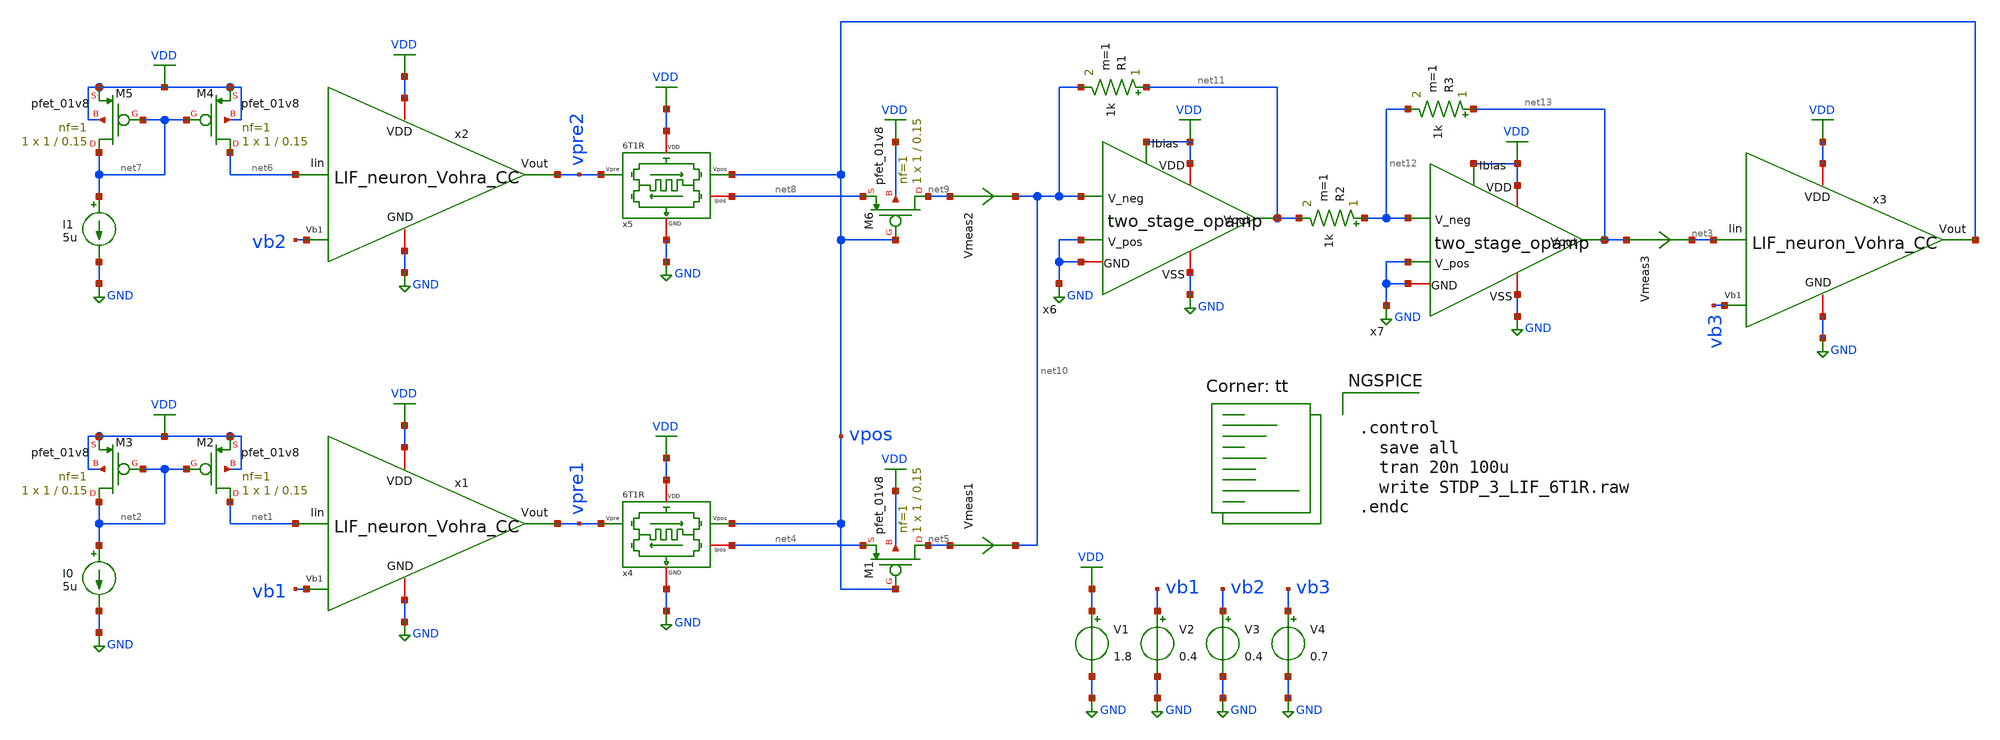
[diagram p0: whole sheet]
** sch_path: STDP/STDP_3_LIF_6T1R_opamps.sch
**.subckt STDP_3_LIF_6T1R_opamps
V1 VDD GND 1.8
V2 vb1 GND 0.4
x4 VDD net4 vpre1 vpos GND 6T1R
x1 VDD vpre1 vb1 GND net1 LIF_neuron_Vohra_CC
I0 net2 GND 5u
XM2 net1 net2 VDD VDD sky130_fd_pr__pfet_01v8 L=0.15 W=1 nf=1 ad='int((nf+1)/2) * W/nf * 0.29' as='int((nf+2)/2) * W/nf * 0.29'
+ pd='2*int((nf+1)/2) * (W/nf + 0.29)' ps='2*int((nf+2)/2) * (W/nf + 0.29)' nrd='0.29 / W' nrs='0.29 / W'
+ sa=0 sb=0 sd=0 mult=1 m=1
XM3 net2 net2 VDD VDD sky130_fd_pr__pfet_01v8 L=0.15 W=1 nf=1 ad='int((nf+1)/2) * W/nf * 0.29' as='int((nf+2)/2) * W/nf * 0.29'
+ pd='2*int((nf+1)/2) * (W/nf + 0.29)' ps='2*int((nf+2)/2) * (W/nf + 0.29)' nrd='0.29 / W' nrs='0.29 / W'
+ sa=0 sb=0 sd=0 mult=1 m=1
x3 VDD vpos vb3 GND net3 LIF_neuron_Vohra_CC
XM1 net5 vpos net4 VDD sky130_fd_pr__pfet_01v8 L=0.15 W=1 nf=1 ad='int((nf+1)/2) * W/nf * 0.29' as='int((nf+2)/2) * W/nf * 0.29'
+ pd='2*int((nf+1)/2) * (W/nf + 0.29)' ps='2*int((nf+2)/2) * (W/nf + 0.29)' nrd='0.29 / W' nrs='0.29 / W'
+ sa=0 sb=0 sd=0 mult=1 m=1
Vmeas1 net5 net10 0
.save i(vmeas1)
V3 vb2 GND 0.4
x5 VDD net8 vpre2 vpos GND 6T1R
x2 VDD vpre2 vb2 GND net6 LIF_neuron_Vohra_CC
I1 net7 GND 5u
XM4 net6 net7 VDD VDD sky130_fd_pr__pfet_01v8 L=0.15 W=1 nf=1 ad='int((nf+1)/2) * W/nf * 0.29' as='int((nf+2)/2) * W/nf * 0.29'
+ pd='2*int((nf+1)/2) * (W/nf + 0.29)' ps='2*int((nf+2)/2) * (W/nf + 0.29)' nrd='0.29 / W' nrs='0.29 / W'
+ sa=0 sb=0 sd=0 mult=1 m=1
XM5 net7 net7 VDD VDD sky130_fd_pr__pfet_01v8 L=0.15 W=1 nf=1 ad='int((nf+1)/2) * W/nf * 0.29' as='int((nf+2)/2) * W/nf * 0.29'
+ pd='2*int((nf+1)/2) * (W/nf + 0.29)' ps='2*int((nf+2)/2) * (W/nf + 0.29)' nrd='0.29 / W' nrs='0.29 / W'
+ sa=0 sb=0 sd=0 mult=1 m=1
XM6 net9 vpos net8 VDD sky130_fd_pr__pfet_01v8 L=0.15 W=1 nf=1 ad='int((nf+1)/2) * W/nf * 0.29' as='int((nf+2)/2) * W/nf * 0.29'
+ pd='2*int((nf+1)/2) * (W/nf + 0.29)' ps='2*int((nf+2)/2) * (W/nf + 0.29)' nrd='0.29 / W' nrs='0.29 / W'
+ sa=0 sb=0 sd=0 mult=1 m=1
Vmeas2 net9 net10 0
.save i(vmeas2)
V4 vb3 GND 0.7
x6 VDD net11 VDD net10 GND GND GND two_stage_opamp W1=15 W2=94 W3=3 W4=4.5 W5=14 W6=10 L1=0.15
+ L2=0.15 L3=0.15 L4=0.15 L5=0.15 L6=0.15
R1 net11 net10 1k m=1
R2 net12 net11 1k m=1
x7 VDD net13 VDD net12 GND GND GND two_stage_opamp W1=15 W2=94 W3=3 W4=4.5 W5=14 W6=10 L1=0.15
+ L2=0.15 L3=0.15 L4=0.15 L5=0.15 L6=0.15
R3 net13 net12 1k m=1
Vmeas3 net13 net3 0
.save i(vmeas3)
**** begin user architecture code
.lib $::SKYWATER_MODELS/sky130.lib.spice tt

** opencircuitdesign pdks install
.inc $::SKYWATER_MODELS/rram_v0.spice



.control
  save all
  tran 20n 100u
  write STDP_3_LIF_6T1R.raw
.endc


**** end user architecture code
**.ends

* expanding   symbol:  /home/ricardoatt/RATT_repos/Proyectos_xschem/synapse/6T1R.sym # of pins=5
** sym_path: synapse/6T1R.sym
** sch_path: synapse/6T1R.sch
.subckt 6T1R VDD Ipos Vpre Vpos GND
*.ipin Vpre
*.ipin Vpos
*.iopin GND
*.iopin Ipos
*.iopin VDD
XM1 vipre Vpre net1 GND sky130_fd_pr__nfet_01v8 L=0.15 W=10 nf=1 ad='int((nf+1)/2) * W/nf * 0.29' as='int((nf+2)/2) * W/nf * 0.29'
+ pd='2*int((nf+1)/2) * (W/nf + 0.29)' ps='2*int((nf+2)/2) * (W/nf + 0.29)' nrd='0.29 / W' nrs='0.29 / W'
+ sa=0 sb=0 sd=0 mult=1 m=1
XR1 net2 net1 rram_v0
XM3 vipre Vpos net2 GND sky130_fd_pr__nfet_01v8 L=0.15 W=1 nf=1 ad='int((nf+1)/2) * W/nf * 0.29' as='int((nf+2)/2) * W/nf * 0.29'
+ pd='2*int((nf+1)/2) * (W/nf + 0.29)' ps='2*int((nf+2)/2) * (W/nf + 0.29)' nrd='0.29 / W' nrs='0.29 / W'
+ sa=0 sb=0 sd=0 mult=1 m=1
XM6 Ipos vipre VDD VDD sky130_fd_pr__pfet_01v8 L=0.15 W=1 nf=1 ad='int((nf+1)/2) * W/nf * 0.29' as='int((nf+2)/2) * W/nf * 0.29'
+ pd='2*int((nf+1)/2) * (W/nf + 0.29)' ps='2*int((nf+2)/2) * (W/nf + 0.29)' nrd='0.29 / W' nrs='0.29 / W'
+ sa=0 sb=0 sd=0 mult=1 m=1
XM5 vipre vipre VDD VDD sky130_fd_pr__pfet_01v8 L=0.15 W=20 nf=1 ad='int((nf+1)/2) * W/nf * 0.29' as='int((nf+2)/2) * W/nf * 0.29'
+ pd='2*int((nf+1)/2) * (W/nf + 0.29)' ps='2*int((nf+2)/2) * (W/nf + 0.29)' nrd='0.29 / W' nrs='0.29 / W'
+ sa=0 sb=0 sd=0 mult=1 m=1
XM2 net1 Vpos GND GND sky130_fd_pr__nfet_01v8 L=0.15 W=1 nf=1 ad='int((nf+1)/2) * W/nf * 0.29' as='int((nf+2)/2) * W/nf * 0.29'
+ pd='2*int((nf+1)/2) * (W/nf + 0.29)' ps='2*int((nf+2)/2) * (W/nf + 0.29)' nrd='0.29 / W' nrs='0.29 / W'
+ sa=0 sb=0 sd=0 mult=1 m=1
XM4 net2 Vpre GND GND sky130_fd_pr__nfet_01v8 L=0.15 W=10 nf=1 ad='int((nf+1)/2) * W/nf * 0.29' as='int((nf+2)/2) * W/nf * 0.29'
+ pd='2*int((nf+1)/2) * (W/nf + 0.29)' ps='2*int((nf+2)/2) * (W/nf + 0.29)' nrd='0.29 / W' nrs='0.29 / W'
+ sa=0 sb=0 sd=0 mult=1 m=1
.ends


* expanding   symbol:
*+  /home/ricardoatt/RATT_repos/Proyectos_xschem/LIF_neuron/LIF_neuron_Vohra_CC.sym # of pins=5
** sym_path: LIF_neuron/LIF_neuron_Vohra_CC.sym
** sch_path: LIF_neuron/LIF_neuron_Vohra_CC.sch
.subckt LIF_neuron_Vohra_CC VDD Vout Vb1 GND Iin
*.iopin GND
*.ipin Vb1
*.iopin VDD
*.opin Vout
*.ipin Iin
XM13 net2 Vb1 GND GND sky130_fd_pr__nfet_01v8 L=0.5 W=5 nf=1 ad='int((nf+1)/2) * W/nf * 0.29' as='int((nf+2)/2) * W/nf * 0.29'
+ pd='2*int((nf+1)/2) * (W/nf + 0.29)' ps='2*int((nf+2)/2) * (W/nf + 0.29)' nrd='0.29 / W' nrs='0.29 / W'
+ sa=0 sb=0 sd=0 mult=1 m=1
XM12 rc net1 net2 GND sky130_fd_pr__nfet_01v8 L=1 W=1 nf=1 ad='int((nf+1)/2) * W/nf * 0.29' as='int((nf+2)/2) * W/nf * 0.29'
+ pd='2*int((nf+1)/2) * (W/nf + 0.29)' ps='2*int((nf+2)/2) * (W/nf + 0.29)' nrd='0.29 / W' nrs='0.29 / W'
+ sa=0 sb=0 sd=0 mult=1 m=1
XM11 rc net1 VDD VDD sky130_fd_pr__pfet_01v8 L=1 W=1 nf=1 ad='int((nf+1)/2) * W/nf * 0.29' as='int((nf+2)/2) * W/nf * 0.29'
+ pd='2*int((nf+1)/2) * (W/nf + 0.29)' ps='2*int((nf+2)/2) * (W/nf + 0.29)' nrd='0.29 / W' nrs='0.29 / W'
+ sa=0 sb=0 sd=0 mult=1 m=1
XC1 rc GND sky130_fd_pr__cap_mim_m3_1 W=21 L=1 MF=1 m=1
XM14 Iin rc GND GND sky130_fd_pr__nfet_01v8 L=10 W=1 nf=1 ad='int((nf+1)/2) * W/nf * 0.29' as='int((nf+2)/2) * W/nf * 0.29'
+ pd='2*int((nf+1)/2) * (W/nf + 0.29)' ps='2*int((nf+2)/2) * (W/nf + 0.29)' nrd='0.29 / W' nrs='0.29 / W'
+ sa=0 sb=0 sd=0 mult=1 m=1
XC2 Iin GND sky130_fd_pr__cap_mim_m3_1 W=10 L=1 MF=50 m=50
XM6 net3 Vout GND GND sky130_fd_pr__nfet_01v8 L=0.5 W=1 nf=1 ad='int((nf+1)/2) * W/nf * 0.29' as='int((nf+2)/2) * W/nf * 0.29'
+ pd='2*int((nf+1)/2) * (W/nf + 0.29)' ps='2*int((nf+2)/2) * (W/nf + 0.29)' nrd='0.29 / W' nrs='0.29 / W'
+ sa=0 sb=0 sd=0 mult=1 m=1
XM7 net1 Iin net3 GND sky130_fd_pr__nfet_01v8 L=1 W=1 nf=1 ad='int((nf+1)/2) * W/nf * 0.29' as='int((nf+2)/2) * W/nf * 0.29'
+ pd='2*int((nf+1)/2) * (W/nf + 0.29)' ps='2*int((nf+2)/2) * (W/nf + 0.29)' nrd='0.29 / W' nrs='0.29 / W'
+ sa=0 sb=0 sd=0 mult=1 m=1
XM8 net1 Iin VDD VDD sky130_fd_pr__pfet_01v8 L=1 W=1 nf=1 ad='int((nf+1)/2) * W/nf * 0.29' as='int((nf+2)/2) * W/nf * 0.29'
+ pd='2*int((nf+1)/2) * (W/nf + 0.29)' ps='2*int((nf+2)/2) * (W/nf + 0.29)' nrd='0.29 / W' nrs='0.29 / W'
+ sa=0 sb=0 sd=0 mult=1 m=1
XM9 Vout net1 net3 GND sky130_fd_pr__nfet_01v8 L=1 W=1 nf=1 ad='int((nf+1)/2) * W/nf * 0.29' as='int((nf+2)/2) * W/nf * 0.29'
+ pd='2*int((nf+1)/2) * (W/nf + 0.29)' ps='2*int((nf+2)/2) * (W/nf + 0.29)' nrd='0.29 / W' nrs='0.29 / W'
+ sa=0 sb=0 sd=0 mult=1 m=1
XM10 Vout net1 VDD VDD sky130_fd_pr__pfet_01v8 L=1 W=5 nf=1 ad='int((nf+1)/2) * W/nf * 0.29' as='int((nf+2)/2) * W/nf * 0.29'
+ pd='2*int((nf+1)/2) * (W/nf + 0.29)' ps='2*int((nf+2)/2) * (W/nf + 0.29)' nrd='0.29 / W' nrs='0.29 / W'
+ sa=0 sb=0 sd=0 mult=1 m=1
.ends


* expanding   symbol:  /home/ricardo/RATT_repos/Proyectos_xschem/two_stage_opamp/two_stage_opamp.sym
*+ # of pins=7
** sym_path: two_stage_opamp/two_stage_opamp.sym
** sch_path: two_stage_opamp/two_stage_opamp.sch
.subckt two_stage_opamp VDD Vout Ibias V_neg GND V_pos VSS  W1=15 W2=94 W3=3 W4=4.5 W5=14 W6=10
+ L1=0.15 L2=0.15 L3=0.15 L4=0.15 L5=0.15 L6=0.15
*.ipin Ibias
*.ipin V_neg
*.ipin V_pos
*.iopin VDD
*.iopin VSS
*.opin Vout
*.iopin GND
XM1 net2 V_neg net4 VSS sky130_fd_pr__nfet_01v8 L=L3 W=W3 nf=1 ad='int((nf+1)/2) * W/nf * 0.29' as='int((nf+2)/2) * W/nf * 0.29'
+ pd='2*int((nf+1)/2) * (W/nf + 0.29)' ps='2*int((nf+2)/2) * (W/nf + 0.29)' nrd='0.29 / W' nrs='0.29 / W'
+ sa=0 sb=0 sd=0 mult=1 m=1
XM3 net2 net2 VDD VDD sky130_fd_pr__pfet_01v8 L=L1 W=W1 nf=1 ad='int((nf+1)/2) * W/nf * 0.29' as='int((nf+2)/2) * W/nf * 0.29'
+ pd='2*int((nf+1)/2) * (W/nf + 0.29)' ps='2*int((nf+2)/2) * (W/nf + 0.29)' nrd='0.29 / W' nrs='0.29 / W'
+ sa=0 sb=0 sd=0 mult=1 m=1
XM2 net3 V_pos net4 VSS sky130_fd_pr__nfet_01v8 L=L3 W=W3 nf=1 ad='int((nf+1)/2) * W/nf * 0.29' as='int((nf+2)/2) * W/nf * 0.29'
+ pd='2*int((nf+1)/2) * (W/nf + 0.29)' ps='2*int((nf+2)/2) * (W/nf + 0.29)' nrd='0.29 / W' nrs='0.29 / W'
+ sa=0 sb=0 sd=0 mult=1 m=1
XM4 net3 net2 VDD VDD sky130_fd_pr__pfet_01v8 L=L1 W=W1 nf=1 ad='int((nf+1)/2) * W/nf * 0.29' as='int((nf+2)/2) * W/nf * 0.29'
+ pd='2*int((nf+1)/2) * (W/nf + 0.29)' ps='2*int((nf+2)/2) * (W/nf + 0.29)' nrd='0.29 / W' nrs='0.29 / W'
+ sa=0 sb=0 sd=0 mult=1 m=1
XM5 net4 net1 VSS VSS sky130_fd_pr__nfet_01v8 L=L4 W=W4 nf=1 ad='int((nf+1)/2) * W/nf * 0.29' as='int((nf+2)/2) * W/nf * 0.29'
+ pd='2*int((nf+1)/2) * (W/nf + 0.29)' ps='2*int((nf+2)/2) * (W/nf + 0.29)' nrd='0.29 / W' nrs='0.29 / W'
+ sa=0 sb=0 sd=0 mult=1 m=1
XM6 Vout net3 VDD VDD sky130_fd_pr__pfet_01v8 L=L2 W=W2 nf=1 ad='int((nf+1)/2) * W/nf * 0.29' as='int((nf+2)/2) * W/nf * 0.29'
+ pd='2*int((nf+1)/2) * (W/nf + 0.29)' ps='2*int((nf+2)/2) * (W/nf + 0.29)' nrd='0.29 / W' nrs='0.29 / W'
+ sa=0 sb=0 sd=0 mult=1 m=1
XM7 Vout net1 VSS VSS sky130_fd_pr__nfet_01v8 L=L5 W=W5 nf=1 ad='int((nf+1)/2) * W/nf * 0.29' as='int((nf+2)/2) * W/nf * 0.29'
+ pd='2*int((nf+1)/2) * (W/nf + 0.29)' ps='2*int((nf+2)/2) * (W/nf + 0.29)' nrd='0.29 / W' nrs='0.29 / W'
+ sa=0 sb=0 sd=0 mult=1 m=1
XM8 net1 net1 VSS VSS sky130_fd_pr__nfet_01v8 L=L4 W=W4 nf=1 ad='int((nf+1)/2) * W/nf * 0.29' as='int((nf+2)/2) * W/nf * 0.29'
+ pd='2*int((nf+1)/2) * (W/nf + 0.29)' ps='2*int((nf+2)/2) * (W/nf + 0.29)' nrd='0.29 / W' nrs='0.29 / W'
+ sa=0 sb=0 sd=0 mult=1 m=1
XM9 net1 net1 Ibias Ibias sky130_fd_pr__pfet_01v8 L=L6 W=W6 nf=1 ad='int((nf+1)/2) * W/nf * 0.29' as='int((nf+2)/2) * W/nf * 0.29'
+ pd='2*int((nf+1)/2) * (W/nf + 0.29)' ps='2*int((nf+2)/2) * (W/nf + 0.29)' nrd='0.29 / W' nrs='0.29 / W'
+ sa=0 sb=0 sd=0 mult=1 m=1
XC1 net3 Vout sky130_fd_pr__cap_mim_m3_1 W=10 L=1 MF=1 m=1
.ends

.GLOBAL GND
.GLOBAL VDD
.end
